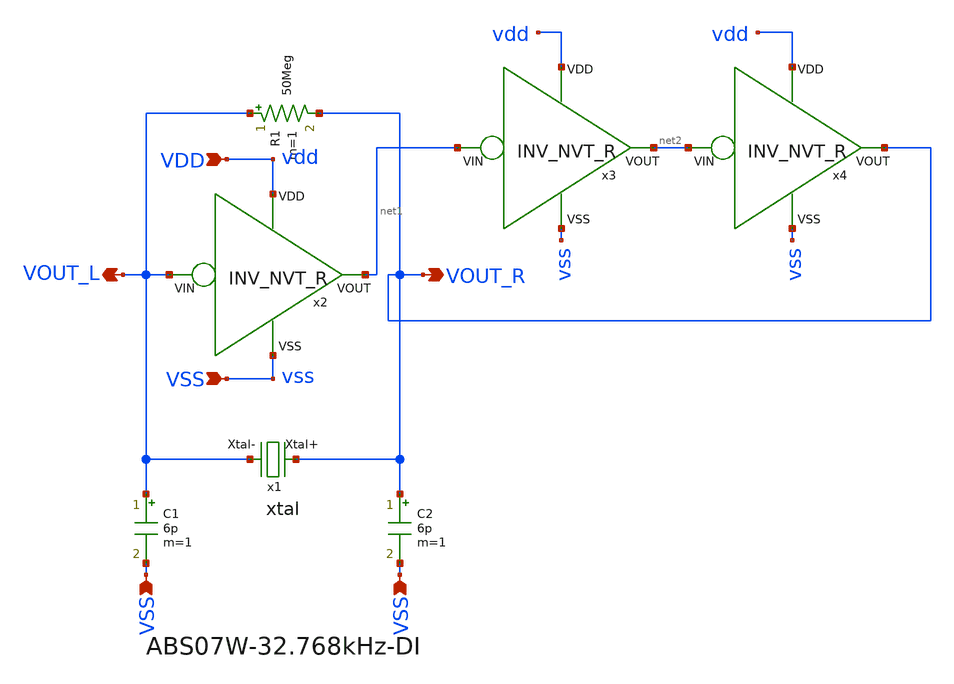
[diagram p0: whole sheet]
** sch_path: design/THESIS_EXP_RO_INVERTER_SKY130A/xtal_osc_nvt_r.sch
**.subckt xtal_osc_nvt_r VDD VSS VSS VSS VOUT_R VOUT_L
*.ipin VDD
*.ipin VSS
*.ipin VSS
*.ipin VSS
*.opin VOUT_R
*.opin VOUT_L
x1 VOUT_R VOUT_L xtal
C1 VOUT_L VSS 6p m=1
C2 VOUT_R VSS 6p m=1
R1 VOUT_L VOUT_R 50Meg m=1
x2 VDD net1 VOUT_L VSS INV_NVT_R
x3 vdd net2 net1 vss INV_NVT_R
x4 vdd VOUT_R net2 vss INV_NVT_R
**.ends

* expanding   symbol:  THESIS_EXP_RO_INVERTER_SKY130A/xtal.sym # of pins=2
** sym_path: design/THESIS_EXP_RO_INVERTER_SKY130A/xtal.sym
** sch_path: design/THESIS_EXP_RO_INVERTER_SKY130A/xtal.sch
.subckt xtal Xtal+ Xtal-
*.iopin Xtal+
*.iopin Xtal-
R1 Xtal+ net1 38.194k m=1
C1 net1 net2 4.68f m=1
L1 net2 Xtal- 5048.571 m=1
C2 Xtal+ Xtal- 1.15p m=1
.ends


* expanding   symbol:  THESIS_EXP_RO_INVERTER_SKY130A/INV_NVT_R.sym # of pins=4
** sym_path: design/THESIS_EXP_RO_INVERTER_SKY130A/INV_NVT_R.sym
** sch_path: design/THESIS_EXP_RO_INVERTER_SKY130A/INV_NVT_R.sch
.subckt INV_NVT_R VDD VOUT VIN VSS
*.ipin VDD
*.ipin VSS
*.ipin VIN
*.opin VOUT
R1 net1 VOUT 1k m=1
XM1 VOUT VIN VSS VSS sky130_fd_pr__nfet_03v3_nvt L=0.6 W=4 nf=1 ad='int((nf+1)/2) * W/nf * 0.29' as='int((nf+2)/2) * W/nf * 0.29'
+ pd='2*int((nf+1)/2) * (W/nf + 0.29)' ps='2*int((nf+2)/2) * (W/nf + 0.29)' nrd='0.29 / W' nrs='0.29 / W'
+ sa=0 sb=0 sd=0 mult=1 m=1
V1 VDD net1 0
.save i(v1)
.ends

.end
